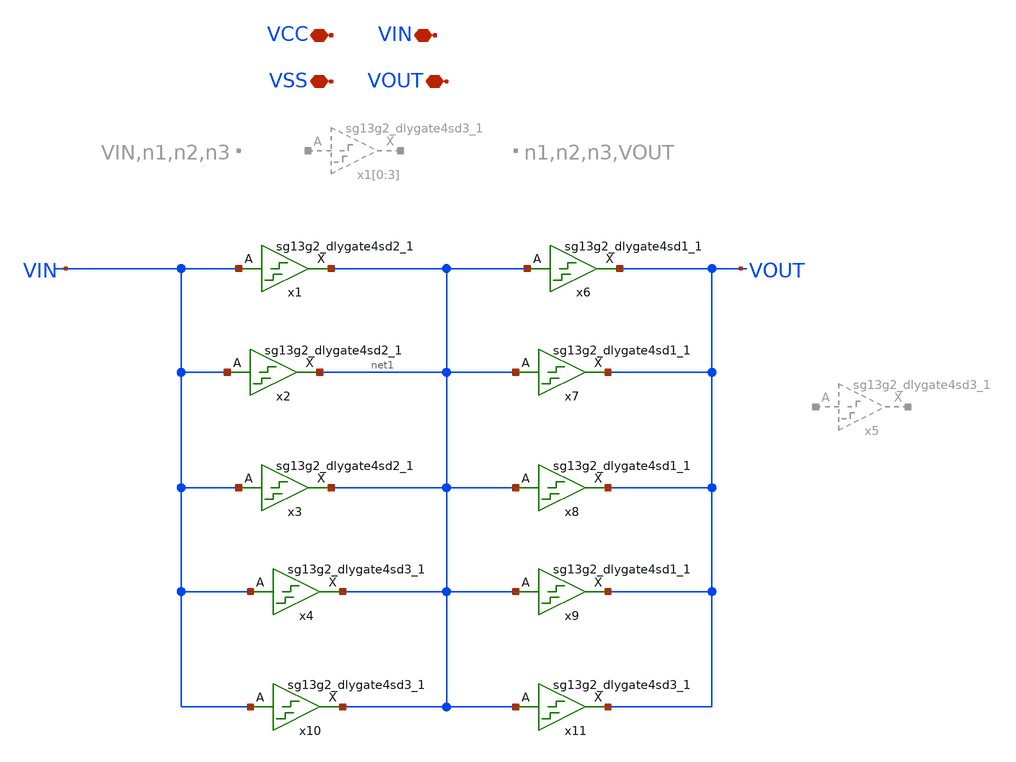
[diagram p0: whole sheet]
** sch_path: sch/large_delay_vto1p1/large_delay_vto1p1.sch
* IHP-GmbH/IHP-Open-PDK/ihp-sg13g2/libs.tech/xschem/sg13g2_stdcells/sg13g2_dlygate4sd2_1.sch:
* Copyright 2023 IHP PDK Authors
* Licensed under the Apache License, Version 2.0 (the "License");
**.subckt large_delay_vto1p1 VIN VOUT VCC VSS
*.iopin VIN
*.iopin VOUT
*.iopin VCC
*.iopin VSS
x1 net1 VIN VCC VSS sg13g2_dlygate4sd2_1
x2 net1 VIN VCC VSS sg13g2_dlygate4sd2_1
x3 net1 VIN VCC VSS sg13g2_dlygate4sd2_1
x4 net1 VIN VCC VSS sg13g2_dlygate4sd3_1
x6 VOUT net1 VCC VSS sg13g2_dlygate4sd1_1
x7 VOUT net1 VCC VSS sg13g2_dlygate4sd1_1
x8 VOUT net1 VCC VSS sg13g2_dlygate4sd1_1
x9 VOUT net1 VCC VSS sg13g2_dlygate4sd1_1
x10 net1 VIN VCC VSS sg13g2_dlygate4sd3_1
x11 VOUT net1 VCC VSS sg13g2_dlygate4sd3_1
**.ends

* expanding   symbol:  sg13g2_stdcells/sg13g2_dlygate4sd3_1.sym # of pins=2
** sym_path: sg13g2_stdcells/sg13g2_dlygate4sd3_1.sym
** sch_path: sg13g2_stdcells/sg13g2_dlygate4sd3_1.sch
.subckt sg13g2_dlygate4sd3_1 X A VDD VSS
*.ipin A
*.opin X
*.iopin VDD
*.iopin VSS
XM1 net3 A VSS VSS sg13_lv_nmos w=420.00n l=130.00n ng=1 m=1 mm_ok=1
XM2 net1 net3 VSS VSS sg13_lv_nmos w=420.00n l=500.0n ng=1 m=1 mm_ok=1
XM3 net2 net1 VSS VSS sg13_lv_nmos w=420.00n l=500.0n ng=1 m=1 mm_ok=1
XM4 X net2 VSS VSS sg13_lv_nmos w=740.00n l=130.00n ng=1 m=1 mm_ok=1
XM5 net3 A VDD VDD sg13_lv_pmos w=420.00n l=130.00n ng=1 m=1 mm_ok=1
XM6 net1 net3 VDD VDD sg13_lv_pmos w=1.000u l=500.0n ng=1 m=1 mm_ok=1
XM7 net2 net1 VDD VDD sg13_lv_pmos w=1.000u l=500.0n ng=1 m=1 mm_ok=1
XM8 X net2 VDD VDD sg13_lv_pmos w=1.12u l=130.00n ng=1 m=1 mm_ok=1
.ends


* expanding   symbol:  sg13g2_stdcells/sg13g2_dlygate4sd2_1.sym # of pins=2
** sym_path: sg13g2_stdcells/sg13g2_dlygate4sd2_1.sym
** sch_path: sg13g2_stdcells/sg13g2_dlygate4sd2_1.sch
.subckt sg13g2_dlygate4sd2_1 X A VDD VSS
*.ipin A
*.opin X
*.iopin VDD
*.iopin VSS
XM1 net2 A VSS VSS sg13_lv_nmos w=420.00n l=130.00n ng=1 m=1 mm_ok=1
XM2 net1 net2 VSS VSS sg13_lv_nmos w=420.00n l=180.00n ng=1 m=1 mm_ok=1
XM3 net3 net1 VSS VSS sg13_lv_nmos w=420.00n l=180.00n ng=1 m=1 mm_ok=1
XM4 X net3 VSS VSS sg13_lv_nmos w=740.00n l=130.00n ng=1 m=1 mm_ok=1
XM5 net2 A VDD VDD sg13_lv_pmos w=420.00n l=130.00n ng=1 m=1 mm_ok=1
XM6 net1 net2 VDD VDD sg13_lv_pmos w=1.000u l=250.00n ng=1 m=1 mm_ok=1
XM7 net3 net1 VDD VDD sg13_lv_pmos w=1.000u l=250.00n ng=1 m=1 mm_ok=1
XM8 X net3 VDD VDD sg13_lv_pmos w=1.12u l=130.00n ng=1 m=1 mm_ok=1
.ends


* expanding   symbol:  sg13g2_stdcells/sg13g2_dlygate4sd1_1.sym # of pins=2
** sym_path: sg13g2_stdcells/sg13g2_dlygate4sd1_1.sym
** sch_path: sg13g2_stdcells/sg13g2_dlygate4sd1_1.sch
.subckt sg13g2_dlygate4sd1_1 X A VDD VSS
*.ipin A
*.opin X
*.iopin VDD
*.iopin VSS
XM1 net2 A VSS VSS sg13_lv_nmos w=420.00n l=130.00n ng=1 m=1 mm_ok=1
XM2 net1 net2 VSS VSS sg13_lv_nmos w=420.00n l=130.00n ng=1 m=1 mm_ok=1
XM3 net3 net1 VSS VSS sg13_lv_nmos w=420.00n l=130.00n ng=1 m=1 mm_ok=1
XM4 X net3 VSS VSS sg13_lv_nmos w=740.00n l=130.00n ng=1 m=1 mm_ok=1
XM5 net2 A VDD VDD sg13_lv_pmos w=420.00n l=130.00n ng=1 m=1 mm_ok=1
XM6 net1 net2 VDD VDD sg13_lv_pmos w=1.000u l=130.00n ng=1 m=1 mm_ok=1
XM7 net3 net1 VDD VDD sg13_lv_pmos w=1.000u l=130.00n ng=1 m=1 mm_ok=1
XM8 X net3 VDD VDD sg13_lv_pmos w=1.12u l=130.00n ng=1 m=1 mm_ok=1
.ends

.end
